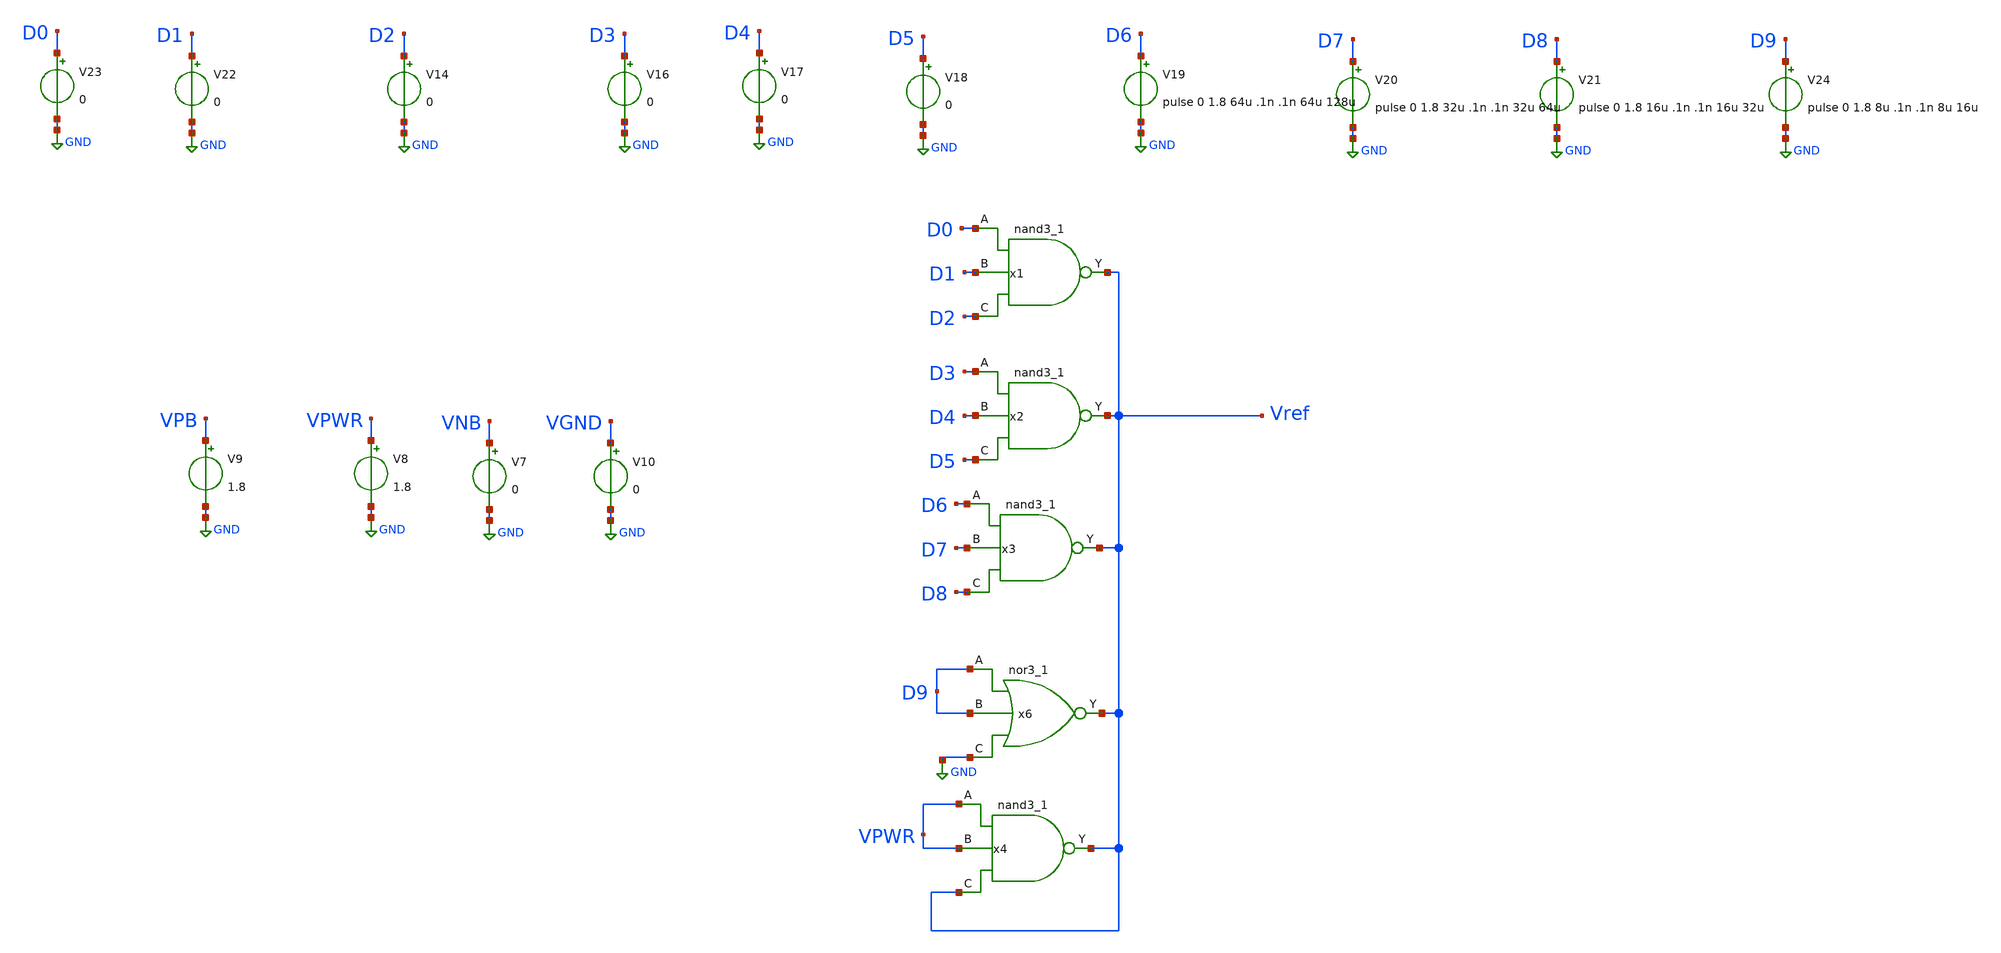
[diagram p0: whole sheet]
** sch_path: DAC/Schematics/DAC.sch
**.subckt DAC
x1 D0 D1 D2 VGND VNB VPB VPWR Vref sky130_fd_sc_hd__nand3_1
x2 D3 D4 D5 VGND VNB VPB VPWR Vref sky130_fd_sc_hd__nand3_1
x3 D6 D7 D8 VGND VNB VPB VPWR Vref sky130_fd_sc_hd__nand3_1
x6 D9 D9 GND VGND VNB VPB VPWR Vref sky130_fd_sc_hd__nor3_1
V7 VNB GND 0
V8 VPWR GND 1.8
V9 VPB GND 1.8
V10 VGND GND 0
x4 VPWR VPWR Vref VGND VNB VPB VPWR Vref sky130_fd_sc_hd__nand3_1
V14 D2 GND 0
V16 D3 GND 0
V17 D4 GND 0
V18 D5 GND 0
V19 D6 GND pulse 0 1.8 64u .1n .1n 64u 128u
V20 D7 GND pulse 0 1.8 32u .1n .1n 32u 64u
V21 D8 GND pulse 0 1.8 16u .1n .1n 16u 32u
V22 D1 GND 0
V23 D0 GND 0
V24 D9 GND pulse 0 1.8 8u .1n .1n 8u 16u
**** begin user architecture code

.include $::SKYWATER_MODELS/cells/nfet_01v8/sky130_fd_pr__nfet_01v8__tt.corner.spice
.include $::SKYWATER_MODELS/cells/nfet_01v8_lvt/sky130_fd_pr__nfet_01v8_lvt__tt.corner.spice
.include $::SKYWATER_MODELS/cells/pfet_01v8/sky130_fd_pr__pfet_01v8__tt.corner.spice
.include $::SKYWATER_MODELS/cells/nfet_03v3_nvt/sky130_fd_pr__nfet_03v3_nvt__tt.corner.spice
.include $::SKYWATER_MODELS/cells/nfet_05v0_nvt/sky130_fd_pr__nfet_05v0_nvt__tt.corner.spice
.include $::SKYWATER_MODELS/cells/esd_nfet_01v8/sky130_fd_pr__esd_nfet_01v8__tt.corner.spice
.include $::SKYWATER_MODELS/cells/pfet_01v8_lvt/sky130_fd_pr__pfet_01v8_lvt__tt.corner.spice
.include $::SKYWATER_MODELS/cells/pfet_01v8_hvt/sky130_fd_pr__pfet_01v8_hvt__tt.corner.spice
.include $::SKYWATER_MODELS/cells/esd_pfet_g5v0d10v5/sky130_fd_pr__esd_pfet_g5v0d10v5__tt.corner.spice
.include $::SKYWATER_MODELS/cells/pfet_g5v0d10v5/sky130_fd_pr__pfet_g5v0d10v5__tt.corner.spice
.include $::SKYWATER_MODELS/cells/pfet_g5v0d16v0/sky130_fd_pr__pfet_g5v0d16v0__tt.corner.spice
.include $::SKYWATER_MODELS/cells/nfet_g5v0d10v5/sky130_fd_pr__nfet_g5v0d10v5__tt.corner.spice
.include $::SKYWATER_MODELS/cells/nfet_g5v0d16v0/sky130_fd_pr__nfet_g5v0d16v0__tt_discrete.corner.spice
.include $::SKYWATER_MODELS/cells/esd_nfet_g5v0d10v5/sky130_fd_pr__esd_nfet_g5v0d10v5__tt.corner.spice
.include $::SKYWATER_MODELS/models/corners/tt/nonfet.spice
* Mismatch parameters
.include $::SKYWATER_MODELS/cells/nfet_01v8/sky130_fd_pr__nfet_01v8__mismatch.corner.spice
.include $::SKYWATER_MODELS/cells/pfet_01v8/sky130_fd_pr__pfet_01v8__mismatch.corner.spice
.include $::SKYWATER_MODELS/cells/nfet_01v8_lvt/sky130_fd_pr__nfet_01v8_lvt__mismatch.corner.spice
.include $::SKYWATER_MODELS/cells/pfet_01v8_lvt/sky130_fd_pr__pfet_01v8_lvt__mismatch.corner.spice
.include $::SKYWATER_MODELS/cells/pfet_01v8_hvt/sky130_fd_pr__pfet_01v8_hvt__mismatch.corner.spice
.include $::SKYWATER_MODELS/cells/nfet_g5v0d10v5/sky130_fd_pr__nfet_g5v0d10v5__mismatch.corner.spice
.include $::SKYWATER_MODELS/cells/pfet_g5v0d10v5/sky130_fd_pr__pfet_g5v0d10v5__mismatch.corner.spice
.include $::SKYWATER_MODELS/cells/nfet_05v0_nvt/sky130_fd_pr__nfet_05v0_nvt__mismatch.corner.spice
.include $::SKYWATER_MODELS/cells/nfet_03v3_nvt/sky130_fd_pr__nfet_03v3_nvt__mismatch.corner.spice
* Resistor$::SKYWATER_MODELS/Capacitor
.include $::SKYWATER_MODELS/models/r+c/res_typical__cap_typical.spice
.include $::SKYWATER_MODELS/models/r+c/res_typical__cap_typical__lin.spice
* Special cells
.include $::SKYWATER_MODELS/models/corners/tt/specialized_cells.spice
* All models
.include $::SKYWATER_MODELS/models/all.spice
* Corner
.include $::SKYWATER_MODELS/models/corners/tt/rf.spice
.include ~/skywater-pdk/libraries/sky130_fd_sc_hd/latest/cells/nand3/sky130_fd_sc_hd__nand3_1.spice
.include ~/skywater-pdk/libraries/sky130_fd_sc_hd/latest/cells/nand2/sky130_fd_sc_hd__nand2_1.spice
.include ~/skywater-pdk/libraries/sky130_fd_sc_hd/latest/cells/nor3/sky130_fd_sc_hd__nor3_1.spice
.include ~/skywater-pdk/libraries/sky130_fd_sc_hd/latest/cells/dfrtp/sky130_fd_sc_hd__dfrtp_1.spice
.include ~/skywater-pdk/libraries/sky130_fd_sc_hd/latest/cells/nor2/sky130_fd_sc_hd__nor2_1.spice
.include ~/skywater-pdk/libraries/sky130_fd_sc_hd/latest/cells/dlrbn/sky130_fd_sc_hd__dlrbn_1.spice
.include ~/skywater-pdk/libraries/sky130_fd_sc_hd/latest/cells/a31o/sky130_fd_sc_hd__a31o_2.spice
.include ~/skywater-pdk/libraries/sky130_fd_sc_hd/latest/cells/inv/sky130_fd_sc_hd__inv_1.spice
.include ~/skywater-pdk/libraries/sky130_fd_sc_hd/latest/cells/a222oi/sky130_fd_sc_hd__a222oi_1.spice
.include ~/skywater-pdk/libraries/sky130_fd_sc_hd/latest/cells/or2/sky130_fd_sc_hd__or2_1.spice
.include ~/skywater-pdk/libraries/sky130_fd_sc_hd/latest/cells/o221ai/sky130_fd_sc_hd__o221ai_1.spice


**** end user architecture code
**.ends
.GLOBAL GND
**** begin user architecture code


.temp 25
vvcc vcc 0 1.8
vvss vss 0 0
.control
tran 10u 1m
plot D0 D1+2 D2+4 D3+6 D4+8 D5+10 D6+12 D7+14 D8+16 D9+18 vref+20
.endc


**** end user architecture code
.end
